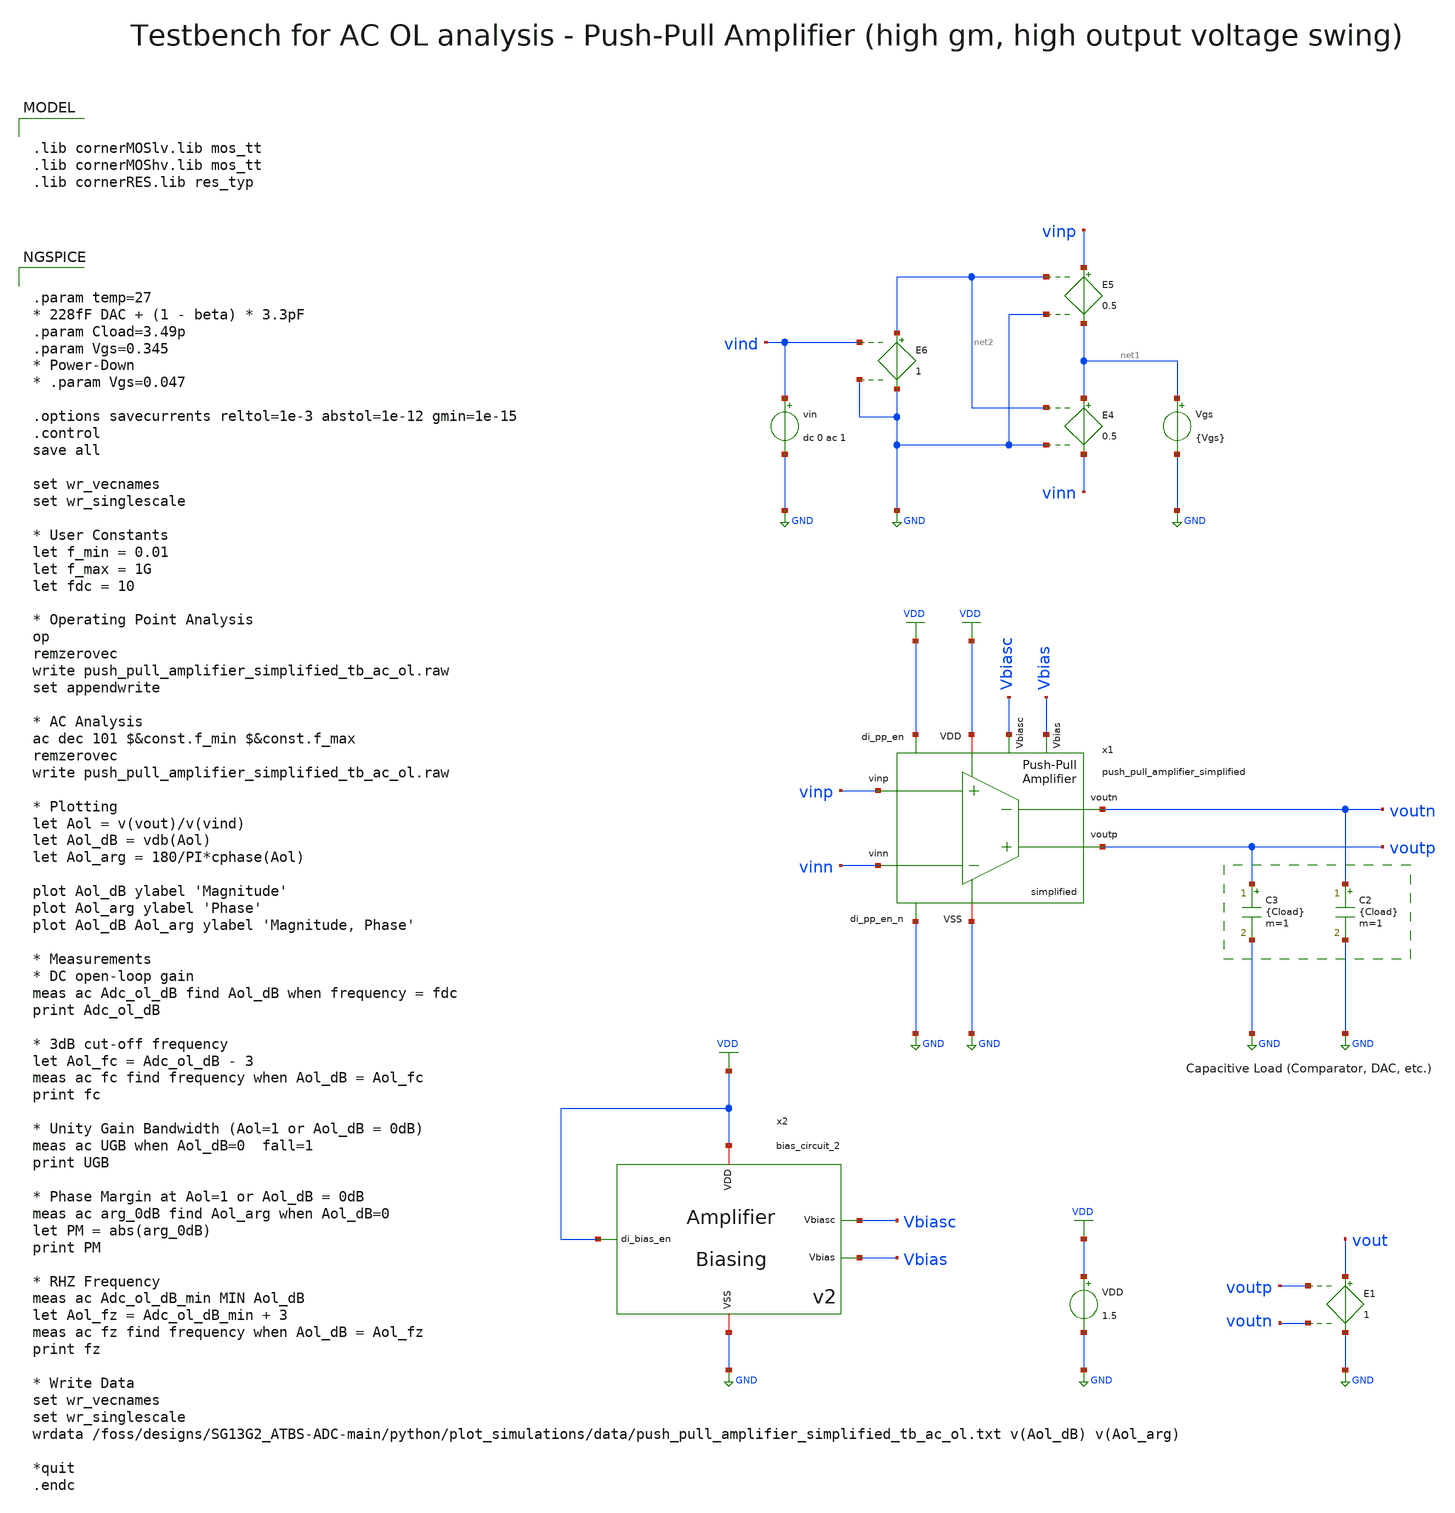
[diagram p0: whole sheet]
** sch_path: SG13G2_ATBS-ADC-main/xschem/bio_amplifier/amplifier_core/push_pull_amplifier/testbenches/push_pull_amplifier_simplified_tb_ac_ol.sch
**.subckt push_pull_amplifier_simplified_tb_ac_ol
VDD VDD GND 1.5
Vgs net1 GND {Vgs}
E4 net1 vinn net2 GND 0.5
E5 vinp net1 net2 GND 0.5
E6 net2 GND vind GND 1
vin vind GND dc 0 ac 1
C2 voutn GND {Cload} m=1
C3 voutp GND {Cload} m=1
E1 vout GND voutp voutn 1
x1 VDD voutp voutn vinn vinp GND GND VDD Vbiasc Vbias push_pull_amplifier_simplified
x2 VDD Vbiasc VDD GND Vbias bias_circuit_2
**** begin user architecture code


.param temp=27
* 228fF DAC + (1 - beta) * 3.3pF
.param Cload=3.49p
.param Vgs=0.345
* Power-Down
* .param Vgs=0.047

.options savecurrents reltol=1e-3 abstol=1e-12 gmin=1e-15
.control
save all

set wr_vecnames
set wr_singlescale

* User Constants
let f_min = 0.01
let f_max = 1G
let fdc = 10

* Operating Point Analysis
op
remzerovec
write push_pull_amplifier_simplified_tb_ac_ol.raw
set appendwrite

* AC Analysis
ac dec 101 $&const.f_min $&const.f_max
remzerovec
write push_pull_amplifier_simplified_tb_ac_ol.raw

* Plotting
let Aol = v(vout)/v(vind)
let Aol_dB = vdb(Aol)
let Aol_arg = 180/PI*cphase(Aol)

plot Aol_dB ylabel 'Magnitude'
plot Aol_arg ylabel 'Phase'
plot Aol_dB Aol_arg ylabel 'Magnitude, Phase'

* Measurements
* DC open-loop gain
meas ac Adc_ol_dB find Aol_dB when frequency = fdc
print Adc_ol_dB

* 3dB cut-off frequency
let Aol_fc = Adc_ol_dB - 3
meas ac fc find frequency when Aol_dB = Aol_fc
print fc

* Unity Gain Bandwidth (Aol=1 or Aol_dB = 0dB)
meas ac UGB when Aol_dB=0  fall=1
print UGB

* Phase Margin at Aol=1 or Aol_dB = 0dB
meas ac arg_0dB find Aol_arg when Aol_dB=0
let PM = abs(arg_0dB)
print PM

* RHZ Frequency
meas ac Adc_ol_dB_min MIN Aol_dB
let Aol_fz = Adc_ol_dB_min + 3
meas ac fz find frequency when Aol_dB = Aol_fz
print fz

* Write Data
set wr_vecnames
set wr_singlescale
wrdata
+ /foss/designs/SG13G2_ATBS-ADC-main/python/plot_simulations/data/push_pull_amplifier_simplified_tb_ac_ol.txt v(Aol_dB) v(Aol_arg)

*quit
.endc



.lib cornerMOSlv.lib mos_tt
.lib cornerMOShv.lib mos_tt
.lib cornerRES.lib res_typ

**** end user architecture code
**.ends
.GLOBAL GND
.GLOBAL VDD
.end
